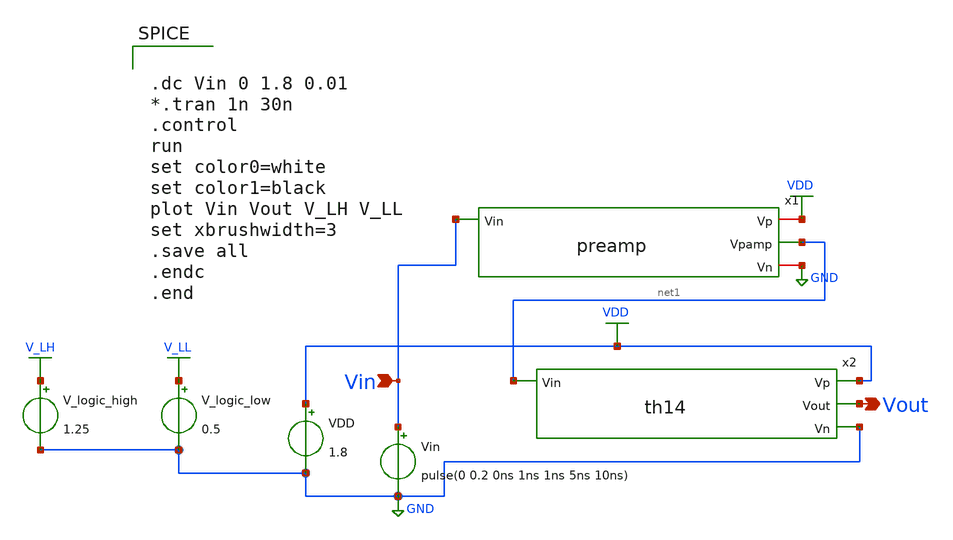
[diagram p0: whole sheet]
** sch_path: xschem/Vth_sch/Pre_layout/th14.sch
**.subckt th14 Vin Vout
*.ipin Vin
*.opin Vout
VDD VDD GND 1.8
Vin Vin GND pulse(0 0.2 0ns 1ns 1ns 5ns 10ns)
V_logic_high V_LH GND 1.25
V_logic_low V_LL GND 0.5
x1 VDD Vin net1 GND preamp
x2 VDD Vout net1 GND th14
**** begin user architecture code


.lib /usr/local/share/pdk/sky130A/libs.tech/ngspice/sky130.lib.spice tt

.save all





.dc Vin 0 1.8 0.01
*.tran 1n 30n
.control
run
set color0=white
set color1=black
plot Vin Vout V_LH V_LL
set xbrushwidth=3
.save all
.endc
.end


**** end user architecture code
**.ends
.GLOBAL VDD
.GLOBAL GND
.GLOBAL V_LH
.GLOBAL V_LL
.end
